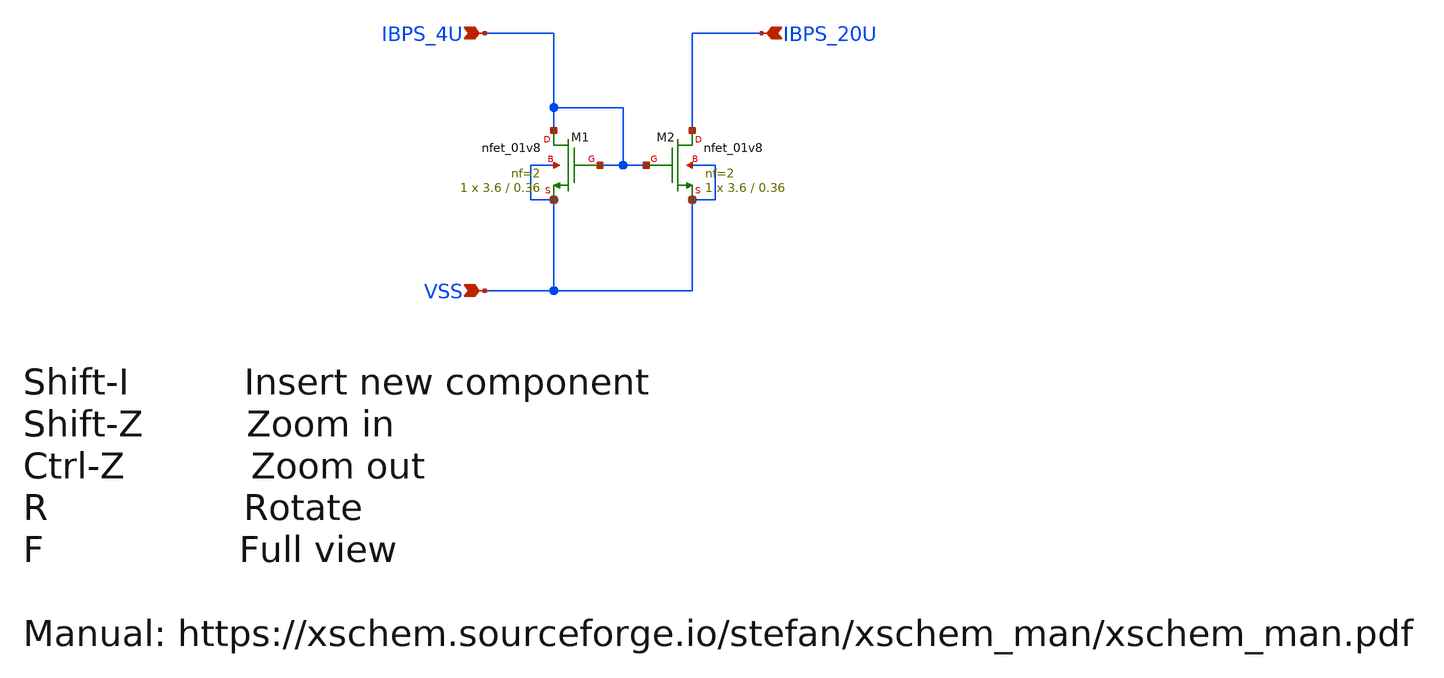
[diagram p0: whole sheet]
** sch_path: design/RPLY_EX0_SKY130NM/RPLY_EX0.sch
**.subckt RPLY_EX0 VSS IBPS_4U IBPS_20U
*.ipin VSS
*.ipin IBPS_4U
*.ipin IBPS_20U
XM2 IBPS_20U IBPS_4U VSS VSS sky130_fd_pr__nfet_01v8 L=0.36 W=3.6 nf=2 ad='int((nf+1)/2) * W/nf * 0.29'
+ as='int((nf+2)/2) * W/nf * 0.29' pd='2*int((nf+1)/2) * (W/nf + 0.29)' ps='2*int((nf+2)/2) * (W/nf + 0.29)'
+ nrd='0.29 / W' nrs='0.29 / W' sa=0 sb=0 sd=0 mult=1 m=1
XM1 IBPS_4U IBPS_4U VSS VSS sky130_fd_pr__nfet_01v8 L=0.36 W=3.6 nf=2 ad='int((nf+1)/2) * W/nf * 0.29'
+ as='int((nf+2)/2) * W/nf * 0.29' pd='2*int((nf+1)/2) * (W/nf + 0.29)' ps='2*int((nf+2)/2) * (W/nf + 0.29)'
+ nrd='0.29 / W' nrs='0.29 / W' sa=0 sb=0 sd=0 mult=1 m=1
**.ends
.end
